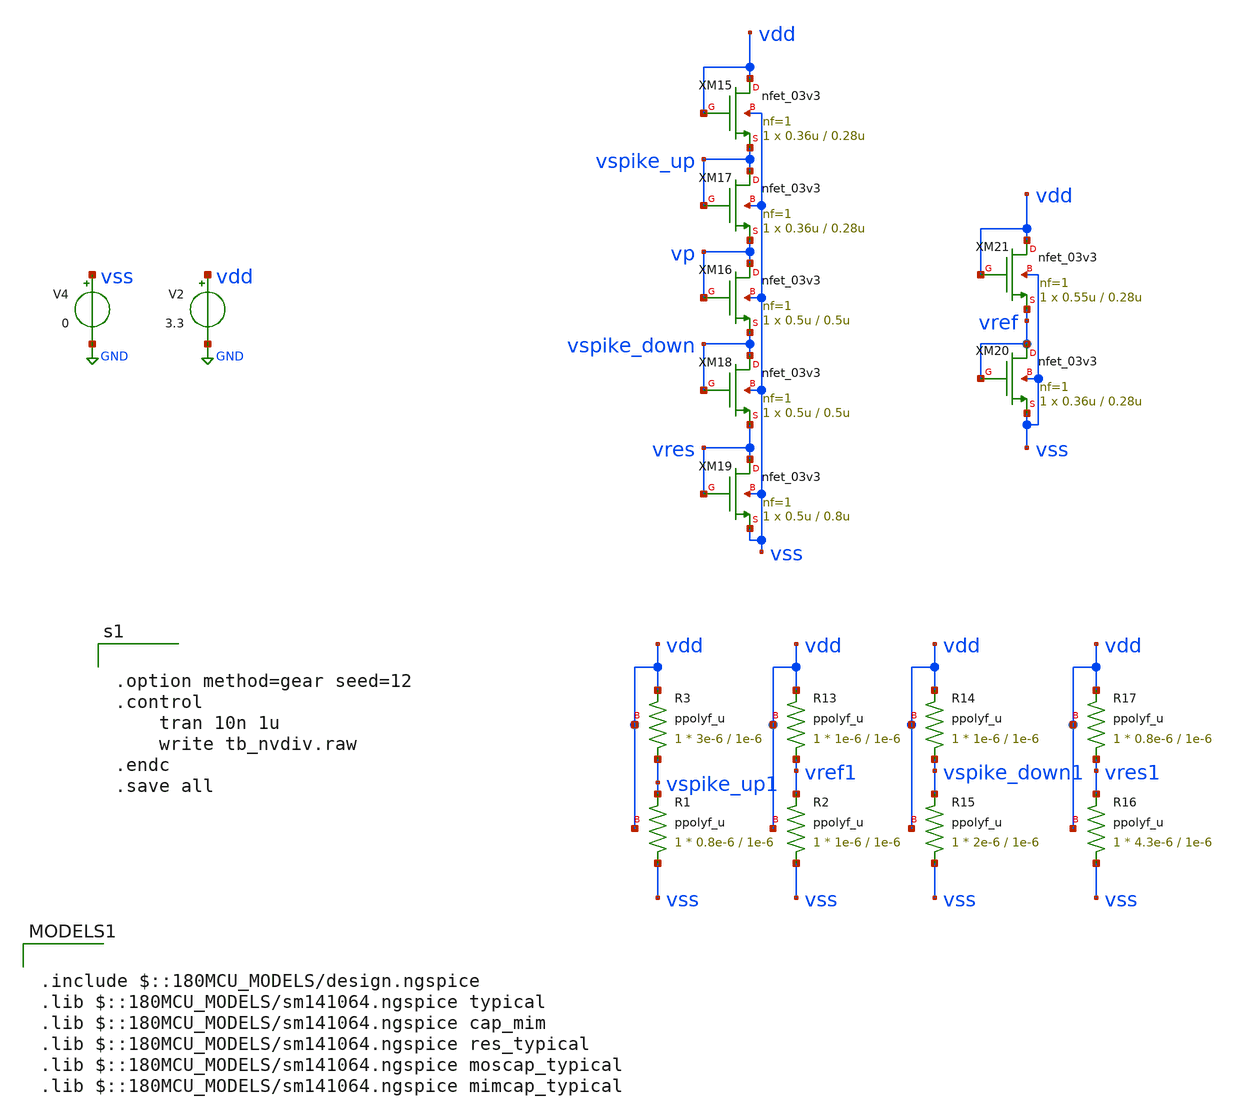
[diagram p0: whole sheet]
** sch_path: designs/libs/core_LIF_comp/tb_nvdiv/tb_nvdiv.sch
**.subckt tb_nvdiv
V2 vdd GND 3.3
V4 vss GND 0
XM15 vdd vdd vspike_up vss nfet_03v3 L=0.28u W=0.36u nf=1 ad='int((nf+1)/2) * W/nf * 0.18u' as='int((nf+2)/2) * W/nf * 0.18u'
+ pd='2*int((nf+1)/2) * (W/nf + 0.18u)' ps='2*int((nf+2)/2) * (W/nf + 0.18u)' nrd='0.18u / W' nrs='0.18u / W'
+ sa=0 sb=0 sd=0 m=1
XM18 vspike_down vspike_down vres vss nfet_03v3 L=0.5u W=0.5u nf=1 ad='int((nf+1)/2) * W/nf * 0.18u'
+ as='int((nf+2)/2) * W/nf * 0.18u' pd='2*int((nf+1)/2) * (W/nf + 0.18u)' ps='2*int((nf+2)/2) * (W/nf + 0.18u)'
+ nrd='0.18u / W' nrs='0.18u / W' sa=0 sb=0 sd=0 m=1
XM16 vp vp vspike_down vss nfet_03v3 L=0.5u W=0.5u nf=1 ad='int((nf+1)/2) * W/nf * 0.18u' as='int((nf+2)/2) * W/nf * 0.18u'
+ pd='2*int((nf+1)/2) * (W/nf + 0.18u)' ps='2*int((nf+2)/2) * (W/nf + 0.18u)' nrd='0.18u / W' nrs='0.18u / W'
+ sa=0 sb=0 sd=0 m=1
XM19 vres vres vss vss nfet_03v3 L=0.8u W=0.5u nf=1 ad='int((nf+1)/2) * W/nf * 0.18u' as='int((nf+2)/2) * W/nf * 0.18u'
+ pd='2*int((nf+1)/2) * (W/nf + 0.18u)' ps='2*int((nf+2)/2) * (W/nf + 0.18u)' nrd='0.18u / W' nrs='0.18u / W'
+ sa=0 sb=0 sd=0 m=1
XM17 vspike_up vspike_up vp vss nfet_03v3 L=0.28u W=0.36u nf=1 ad='int((nf+1)/2) * W/nf * 0.18u' as='int((nf+2)/2) * W/nf * 0.18u'
+ pd='2*int((nf+1)/2) * (W/nf + 0.18u)' ps='2*int((nf+2)/2) * (W/nf + 0.18u)' nrd='0.18u / W' nrs='0.18u / W'
+ sa=0 sb=0 sd=0 m=1
XM20 vref vref vss vss nfet_03v3 L=0.28u W=0.36u nf=1 ad='int((nf+1)/2) * W/nf * 0.18u' as='int((nf+2)/2) * W/nf * 0.18u'
+ pd='2*int((nf+1)/2) * (W/nf + 0.18u)' ps='2*int((nf+2)/2) * (W/nf + 0.18u)' nrd='0.18u / W' nrs='0.18u / W'
+ sa=0 sb=0 sd=0 m=1
XM21 vdd vdd vref vss nfet_03v3 L=0.28u W=0.55u nf=1 ad='int((nf+1)/2) * W/nf * 0.18u' as='int((nf+2)/2) * W/nf * 0.18u'
+ pd='2*int((nf+1)/2) * (W/nf + 0.18u)' ps='2*int((nf+2)/2) * (W/nf + 0.18u)' nrd='0.18u / W' nrs='0.18u / W'
+ sa=0 sb=0 sd=0 m=1
XR3 vspike_up1 vdd vdd ppolyf_u r_width=3e-6 r_length=1e-6 m=1
XR1 vss vspike_up1 vdd ppolyf_u r_width=0.8e-6 r_length=1e-6 m=1
XR2 vss vref1 vdd ppolyf_u r_width=1e-6 r_length=1e-6 m=1
XR13 vref1 vdd vdd ppolyf_u r_width=1e-6 r_length=1e-6 m=1
XR14 vspike_down1 vdd vdd ppolyf_u r_width=1e-6 r_length=1e-6 m=1
XR15 vss vspike_down1 vdd ppolyf_u r_width=2e-6 r_length=1e-6 m=1
XR16 vss vres1 vdd ppolyf_u r_width=4.3e-6 r_length=1e-6 m=1
XR17 vres1 vdd vdd ppolyf_u r_width=0.8e-6 r_length=1e-6 m=1
**** begin user architecture code


.option method=gear seed=12
.control
    tran 10n 1u
    write tb_nvdiv.raw
.endc
.save all



.include $::180MCU_MODELS/design.ngspice
.lib $::180MCU_MODELS/sm141064.ngspice typical
.lib $::180MCU_MODELS/sm141064.ngspice cap_mim
.lib $::180MCU_MODELS/sm141064.ngspice res_typical
.lib $::180MCU_MODELS/sm141064.ngspice moscap_typical
.lib $::180MCU_MODELS/sm141064.ngspice mimcap_typical

**** end user architecture code
**.ends
.GLOBAL GND
.end
